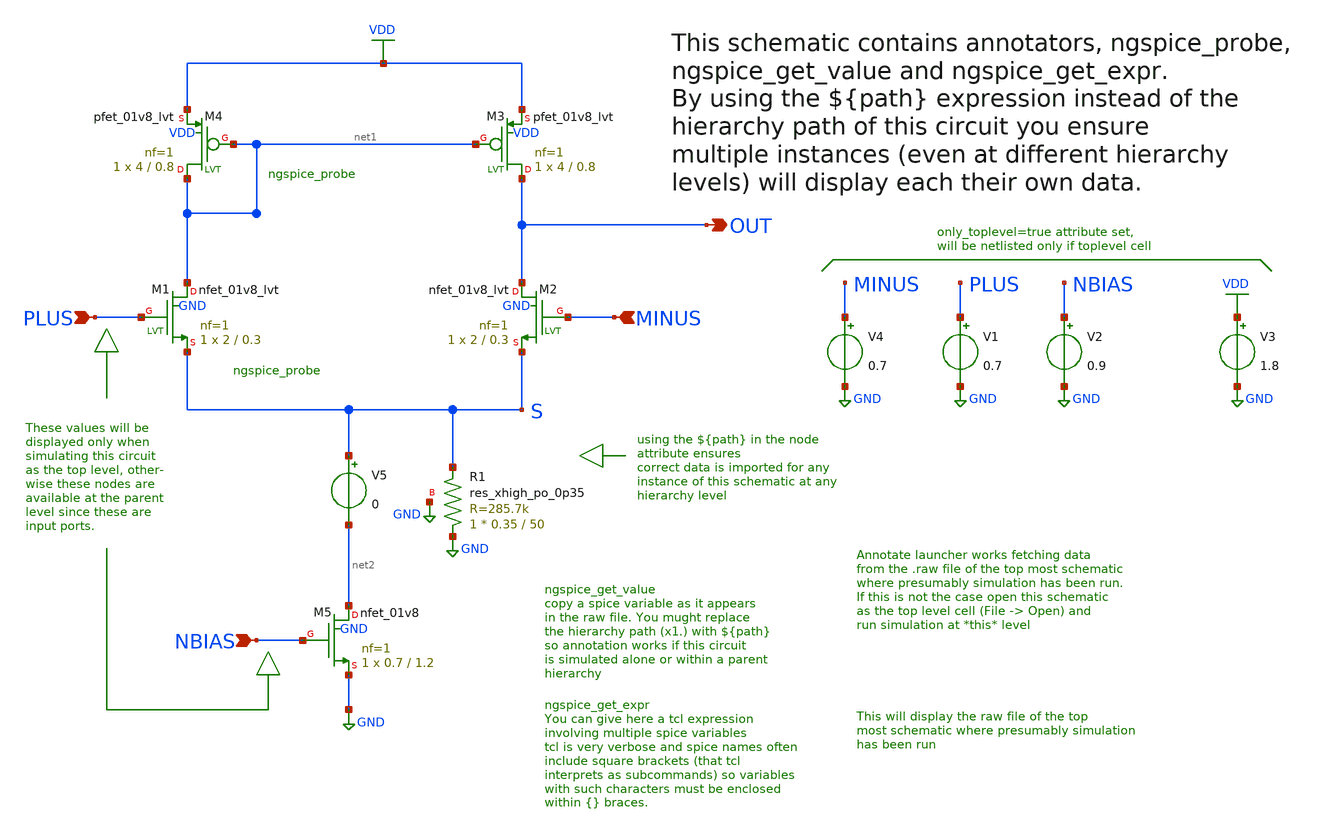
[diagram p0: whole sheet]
** sch_path: sky130_tests/n_diffamp.sch
* Copyright 2021 Stefan Frederik Schippers
* Licensed under the Apache License, Version 2.0 (the "License");
* you may not use this file except in compliance with the License.
* You may obtain a copy of the License at
* https://www.apache.org/licenses/LICENSE-2.0
* Unless required by applicable law or agreed to in writing, software
* distributed under the License is distributed on an "AS IS" BASIS,
* WITHOUT WARRANTIES OR CONDITIONS OF ANY KIND, either express or implied.
* See the License for the specific language governing permissions and
* limitations under the License.
**.subckt n_diffamp PLUS MINUS OUT NBIAS
*.ipin PLUS
*.ipin MINUS
*.opin OUT
*.ipin NBIAS
XM1 net1 PLUS S GND sky130_fd_pr__nfet_01v8_lvt L=0.3 W=2 nf=1 ad='int((nf+1)/2) * W/nf * 0.29' as='int((nf+2)/2) * W/nf * 0.29'
+ pd='2*int((nf+1)/2) * (W/nf + 0.29)' ps='2*int((nf+2)/2) * (W/nf + 0.29)' nrd='0.29 / W' nrs='0.29 / W'
+ sa=0 sb=0 sd=0 mult=1 m=1
XM2 OUT MINUS S GND sky130_fd_pr__nfet_01v8_lvt L=0.3 W=2 nf=1 ad='int((nf+1)/2) * W/nf * 0.29' as='int((nf+2)/2) * W/nf * 0.29'
+ pd='2*int((nf+1)/2) * (W/nf + 0.29)' ps='2*int((nf+2)/2) * (W/nf + 0.29)' nrd='0.29 / W' nrs='0.29 / W'
+ sa=0 sb=0 sd=0 mult=1 m=1
XM3 OUT net1 VDD VDD sky130_fd_pr__pfet_01v8_lvt L=0.8 W=4 nf=1 ad='int((nf+1)/2) * W/nf * 0.29' as='int((nf+2)/2) * W/nf * 0.29'
+ pd='2*int((nf+1)/2) * (W/nf + 0.29)' ps='2*int((nf+2)/2) * (W/nf + 0.29)' nrd='0.29 / W' nrs='0.29 / W'
+ sa=0 sb=0 sd=0 mult=1 m=1
XM4 net1 net1 VDD VDD sky130_fd_pr__pfet_01v8_lvt L=0.8 W=4 nf=1 ad='int((nf+1)/2) * W/nf * 0.29' as='int((nf+2)/2) * W/nf * 0.29'
+ pd='2*int((nf+1)/2) * (W/nf + 0.29)' ps='2*int((nf+2)/2) * (W/nf + 0.29)' nrd='0.29 / W' nrs='0.29 / W'
+ sa=0 sb=0 sd=0 mult=1 m=1
XM5 net2 NBIAS GND GND sky130_fd_pr__nfet_01v8 L=1.2 W=0.7 nf=1 ad='int((nf+1)/2) * W/nf * 0.29' as='int((nf+2)/2) * W/nf * 0.29'
+ pd='2*int((nf+1)/2) * (W/nf + 0.29)' ps='2*int((nf+2)/2) * (W/nf + 0.29)' nrd='0.29 / W' nrs='0.29 / W'
+ sa=0 sb=0 sd=0 mult=1 m=1
XR1 GND S GND sky130_fd_pr__res_xhigh_po_0p35 L=50 mult=1 m=1
V1 PLUS GND 0.7
V2 NBIAS GND 0.9
V3 VDD GND 1.8
V4 MINUS GND 0.7
V5 S net2 0
**** begin user architecture code
 ** manual skywater pdks install (with patches applied)
* .lib $::SKYWATER_MODELS/models/sky130.lib.spice tt

** opencircuitdesign pdks install
.lib $::SKYWATER_MODELS/sky130.lib.spice tt

** manual skywater-pdk install (with patches applied).
* .include $::SKYWATER_MODELS/cells/pnp_05v5/sky130_fd_pr__pnp_05v5_W3p40L3p40.model.spice

** opencircuitdesign pdks install
.include $::SKYWATER_MODELS/../../libs.ref/sky130_fd_pr/spice/sky130_fd_pr__pnp_05v5_W3p40L3p40.model.spice

.param mc_mm_switch=0
.param mc_pr_switch=1

**** end user architecture code
**.ends
.GLOBAL GND
.GLOBAL VDD
**** begin user architecture code

.options savecurrents
.control
save @m.xm5.msky130_fd_pr__nfet_01v8[gm]
save all
op
write n_diffamp.raw
.endc


**** end user architecture code
.end
